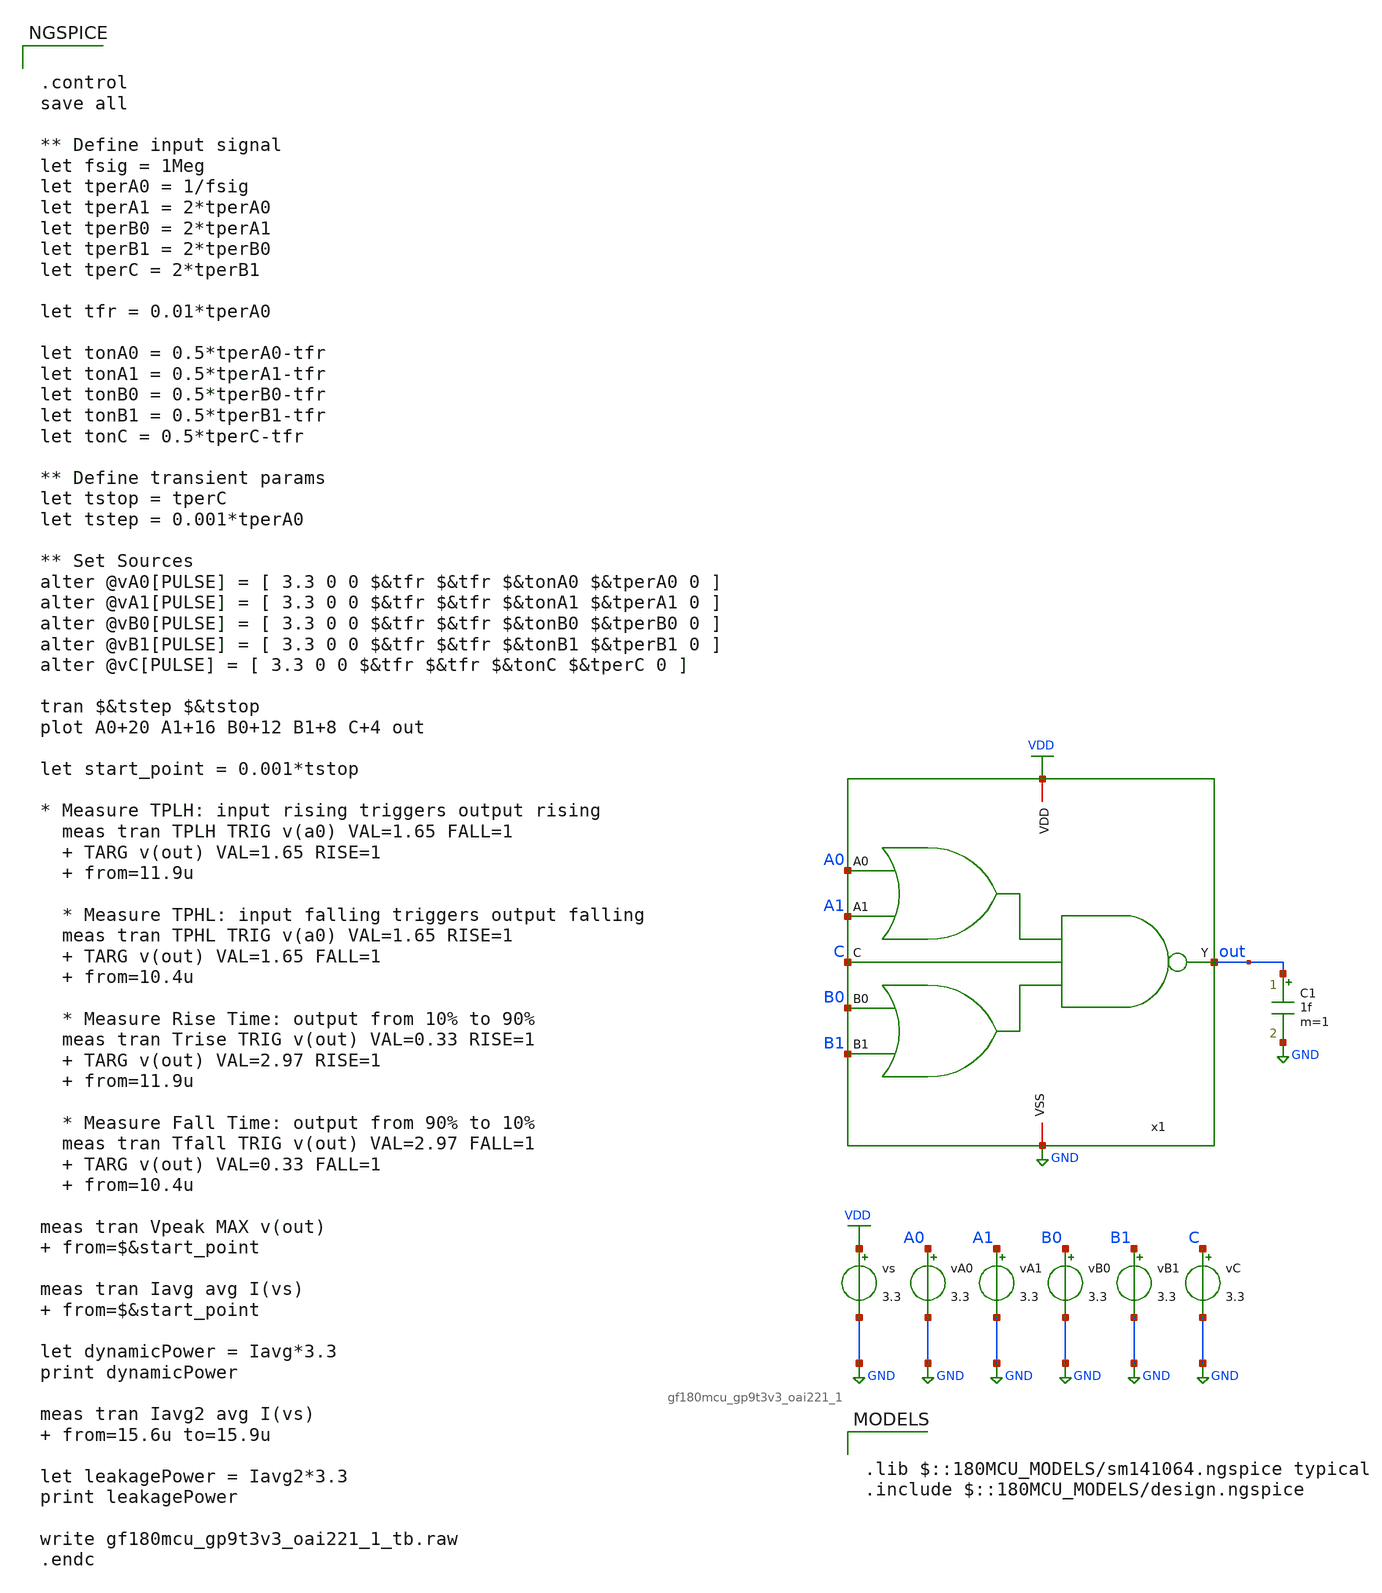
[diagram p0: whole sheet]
** sch_path: designs/oai221/gf180mcu_gp9t3v3_oai221_1_tb.sch
**.subckt gf180mcu_gp9t3v3_oai221_1_tb
vA0 A0 GND 3.3
vs VDD GND 3.3
vA1 A1 GND 3.3
vB1 B1 GND 3.3
vB0 B0 GND 3.3
vC C GND 3.3
C1 out GND 1f m=1
x1 VDD A0 B0 C A1 B1 out GND gf180mcu_gp9t3v3_oai221_1
**** begin user architecture code


.control
save all

** Define input signal
let fsig = 1Meg
let tperA0 = 1/fsig
let tperA1 = 2*tperA0
let tperB0 = 2*tperA1
let tperB1 = 2*tperB0
let tperC = 2*tperB1

let tfr = 0.01*tperA0

let tonA0 = 0.5*tperA0-tfr
let tonA1 = 0.5*tperA1-tfr
let tonB0 = 0.5*tperB0-tfr
let tonB1 = 0.5*tperB1-tfr
let tonC = 0.5*tperC-tfr

** Define transient params
let tstop = tperC
let tstep = 0.001*tperA0

** Set Sources
alter @vA0[PULSE] = [ 3.3 0 0 $&tfr $&tfr $&tonA0 $&tperA0 0 ]
alter @vA1[PULSE] = [ 3.3 0 0 $&tfr $&tfr $&tonA1 $&tperA1 0 ]
alter @vB0[PULSE] = [ 3.3 0 0 $&tfr $&tfr $&tonB0 $&tperB0 0 ]
alter @vB1[PULSE] = [ 3.3 0 0 $&tfr $&tfr $&tonB1 $&tperB1 0 ]
alter @vC[PULSE] = [ 3.3 0 0 $&tfr $&tfr $&tonC $&tperC 0 ]

tran $&tstep $&tstop
plot A0+20 A1+16 B0+12 B1+8 C+4 out

let start_point = 0.001*tstop

* Measure TPLH: input rising triggers output rising
  meas tran TPLH TRIG v(a0) VAL=1.65 FALL=1
  + TARG v(out) VAL=1.65 RISE=1
  + from=11.9u

  * Measure TPHL: input falling triggers output falling
  meas tran TPHL TRIG v(a0) VAL=1.65 RISE=1
  + TARG v(out) VAL=1.65 FALL=1
  + from=10.4u

  * Measure Rise Time: output from 10% to 90%
  meas tran Trise TRIG v(out) VAL=0.33 RISE=1
  + TARG v(out) VAL=2.97 RISE=1
  + from=11.9u

  * Measure Fall Time: output from 90% to 10%
  meas tran Tfall TRIG v(out) VAL=2.97 FALL=1
  + TARG v(out) VAL=0.33 FALL=1
  + from=10.4u

meas tran Vpeak MAX v(out)  from=$&start_point

meas tran Iavg avg I(vs)  from=$&start_point

let dynamicPower = Iavg*3.3
print dynamicPower

meas tran Iavg2 avg I(vs)  from=15.6u to=15.9u

let leakagePower = Iavg2*3.3
print leakagePower

write gf180mcu_gp9t3v3_oai221_1_tb.raw
.endc



.lib $::180MCU_MODELS/sm141064.ngspice typical
.include $::180MCU_MODELS/design.ngspice

**** end user architecture code
**.ends

* expanding   symbol:
*+  ChipiChapa/SSCS-Chipaton-2025_ChipiChapa/designs/oai221/gf180mcu_gp9t3v3_oai221_1.sym # of pins=8
** sym_path: designs/oai221/gf180mcu_gp9t3v3_oai221_1.sym
** sch_path: designs/oai221/gf180mcu_gp9t3v3_oai221_1.sch
.subckt gf180mcu_gp9t3v3_oai221_1 VDD A0 B0 C A1 B1 Y VSS
*.ipin A0
*.ipin A1
*.ipin C
*.ipin B0
*.ipin B1
*.opin Y
*.iopin VSS
*.iopin VDD
XMB0_n net2 B0 VSS VSS nfet_03v3 L=0.3u W=0.85u nf=1 ad='int((nf+1)/2) * W/nf * 0.18u' as='int((nf+2)/2) * W/nf * 0.18u'
+ pd='2*int((nf+1)/2) * (W/nf + 0.18u)' ps='2*int((nf+2)/2) * (W/nf + 0.18u)' nrd='0.18u / W' nrs='0.18u / W'
+ sa=0 sb=0 sd=0 m=1
XMC_p Y C VDD VDD pfet_03v3 L=0.3u W=1.7u nf=1 ad='int((nf+1)/2) * W/nf * 0.18u' as='int((nf+2)/2) * W/nf * 0.18u'
+ pd='2*int((nf+1)/2) * (W/nf + 0.18u)' ps='2*int((nf+2)/2) * (W/nf + 0.18u)' nrd='0.18u / W' nrs='0.18u / W'
+ sa=0 sb=0 sd=0 m=1
XMB1_n net2 B1 VSS VSS nfet_03v3 L=0.3u W=0.85u nf=1 ad='int((nf+1)/2) * W/nf * 0.18u' as='int((nf+2)/2) * W/nf * 0.18u'
+ pd='2*int((nf+1)/2) * (W/nf + 0.18u)' ps='2*int((nf+2)/2) * (W/nf + 0.18u)' nrd='0.18u / W' nrs='0.18u / W'
+ sa=0 sb=0 sd=0 m=1
XMC_n net1 C net2 VSS nfet_03v3 L=0.3u W=0.85u nf=1 ad='int((nf+1)/2) * W/nf * 0.18u' as='int((nf+2)/2) * W/nf * 0.18u'
+ pd='2*int((nf+1)/2) * (W/nf + 0.18u)' ps='2*int((nf+2)/2) * (W/nf + 0.18u)' nrd='0.18u / W' nrs='0.18u / W'
+ sa=0 sb=0 sd=0 m=1
XMA0_n Y A0 net1 VSS nfet_03v3 L=0.3u W=0.85u nf=1 ad='int((nf+1)/2) * W/nf * 0.18u' as='int((nf+2)/2) * W/nf * 0.18u'
+ pd='2*int((nf+1)/2) * (W/nf + 0.18u)' ps='2*int((nf+2)/2) * (W/nf + 0.18u)' nrd='0.18u / W' nrs='0.18u / W'
+ sa=0 sb=0 sd=0 m=1
XMA1_n Y A1 net1 VSS nfet_03v3 L=0.3u W=0.85u nf=1 ad='int((nf+1)/2) * W/nf * 0.18u' as='int((nf+2)/2) * W/nf * 0.18u'
+ pd='2*int((nf+1)/2) * (W/nf + 0.18u)' ps='2*int((nf+2)/2) * (W/nf + 0.18u)' nrd='0.18u / W' nrs='0.18u / W'
+ sa=0 sb=0 sd=0 m=1
XMA1_p Y A1 net3 VDD pfet_03v3 L=0.3u W=1.7u nf=1 ad='int((nf+1)/2) * W/nf * 0.18u' as='int((nf+2)/2) * W/nf * 0.18u'
+ pd='2*int((nf+1)/2) * (W/nf + 0.18u)' ps='2*int((nf+2)/2) * (W/nf + 0.18u)' nrd='0.18u / W' nrs='0.18u / W'
+ sa=0 sb=0 sd=0 m=1
XMB1_p Y B1 net4 VDD pfet_03v3 L=0.3u W=1.7u nf=1 ad='int((nf+1)/2) * W/nf * 0.18u' as='int((nf+2)/2) * W/nf * 0.18u'
+ pd='2*int((nf+1)/2) * (W/nf + 0.18u)' ps='2*int((nf+2)/2) * (W/nf + 0.18u)' nrd='0.18u / W' nrs='0.18u / W'
+ sa=0 sb=0 sd=0 m=1
XMA0_p net3 A0 VDD VDD pfet_03v3 L=0.3u W=1.7u nf=1 ad='int((nf+1)/2) * W/nf * 0.18u' as='int((nf+2)/2) * W/nf * 0.18u'
+ pd='2*int((nf+1)/2) * (W/nf + 0.18u)' ps='2*int((nf+2)/2) * (W/nf + 0.18u)' nrd='0.18u / W' nrs='0.18u / W'
+ sa=0 sb=0 sd=0 m=1
XMB0_p net4 B0 VDD VDD pfet_03v3 L=0.3u W=1.7u nf=1 ad='int((nf+1)/2) * W/nf * 0.18u' as='int((nf+2)/2) * W/nf * 0.18u'
+ pd='2*int((nf+1)/2) * (W/nf + 0.18u)' ps='2*int((nf+2)/2) * (W/nf + 0.18u)' nrd='0.18u / W' nrs='0.18u / W'
+ sa=0 sb=0 sd=0 m=1
.ends

.GLOBAL VDD
.GLOBAL GND
.end
